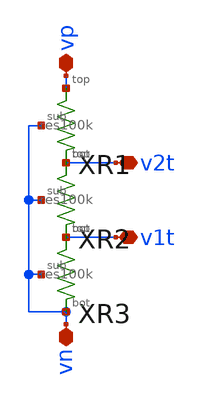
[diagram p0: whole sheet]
** sch_path: xschem/vdiv.sch
**.subckt vdiv vp v2t v1t vn
*.iopin vp
*.iopin v2t
*.iopin v1t
*.iopin vn
XR1 v2t vp vn res100k
XR2 v1t v2t vn res100k
XR3 vn v1t vn res100k
**.ends

* expanding   symbol:  res100k.sym # of pins=3
** sym_path: xschem/res100k.sym
** sch_path: xschem/res100k.sch
.subckt res100k bot top sub
*.iopin top
*.iopin bot
*.iopin sub
XR1 net1 top sub sky130_fd_pr__res_xhigh_po W=0.35 L=3.5 mult=1 m=1
XR2 net2 net1 sub sky130_fd_pr__res_xhigh_po W=0.35 L=3.5 mult=1 m=1
XR3 net3 net2 sub sky130_fd_pr__res_xhigh_po W=0.35 L=3.5 mult=1 m=1
XR4 net4 net3 sub sky130_fd_pr__res_xhigh_po W=0.35 L=3.5 mult=1 m=1
XR5 bot net4 sub sky130_fd_pr__res_xhigh_po W=0.35 L=3.5 mult=1 m=1
.ends

.end
